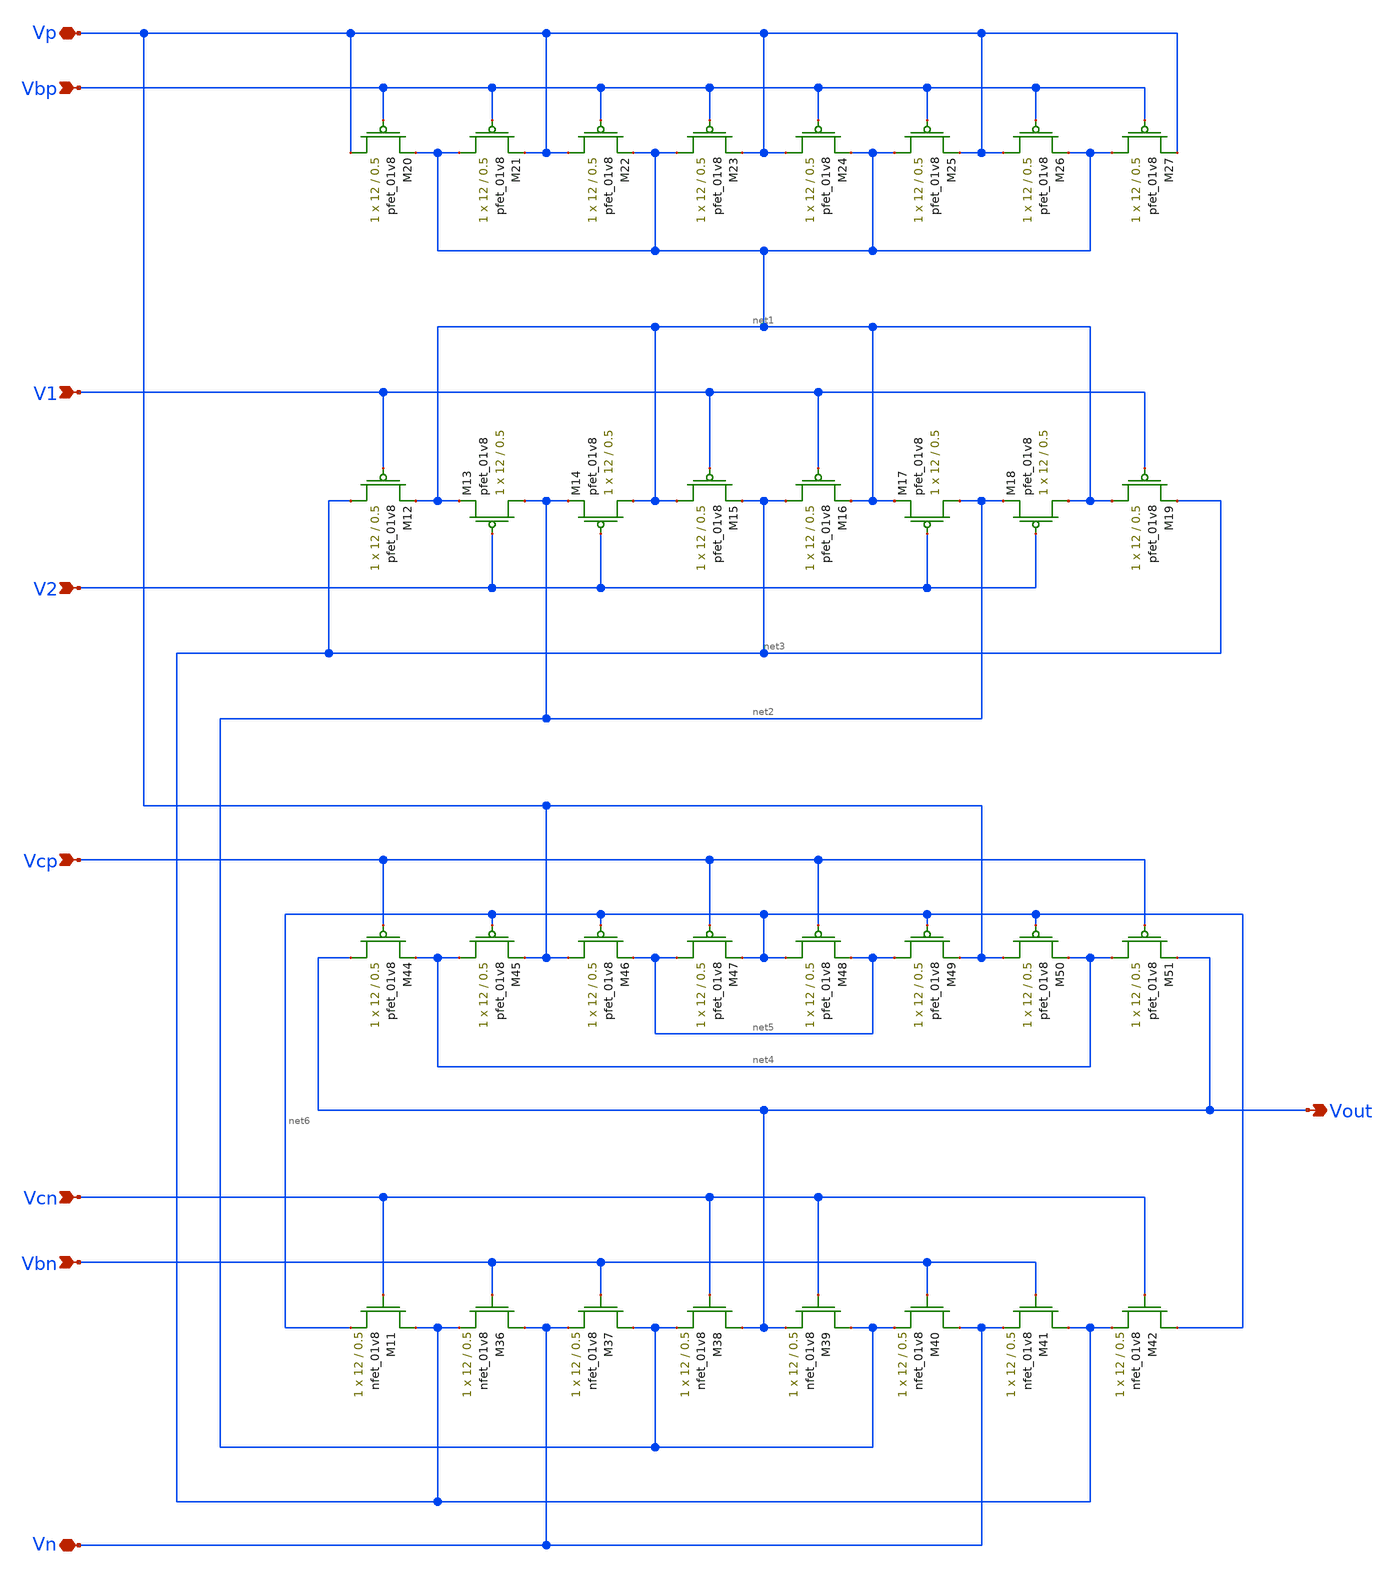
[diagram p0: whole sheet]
** sch_path: schematic/folded_cascode_differential_amplifier_LDS.sch
**.subckt folded_cascode_differential_amplifier_LDS Vbn Vcn Vcp V2 V1 Vbp Vp Vn Vout
*.ipin Vbn
*.ipin Vcn
*.ipin Vcp
*.ipin V2
*.ipin V1
*.ipin Vbp
*.iopin Vp
*.iopin Vn
*.opin Vout
XM11 net3 Vcn net6 GND sky130_fd_pr__nfet_01v8 L=0.5 W=12 nf=1 ad='int((nf+1)/2) * W/nf * 0.29' as='int((nf+2)/2) * W/nf * 0.29'
+ pd='2*int((nf+1)/2) * (W/nf + 0.29)' ps='2*int((nf+2)/2) * (W/nf + 0.29)' nrd='0.29 / W' nrs='0.29 / W'
+ sa=0 sb=0 sd=0 mult=1 m=1
XM12 net3 V1 net1 VDD sky130_fd_pr__pfet_01v8 L=0.5 W=12 nf=1 ad='int((nf+1)/2) * W/nf * 0.29' as='int((nf+2)/2) * W/nf * 0.29'
+ pd='2*int((nf+1)/2) * (W/nf + 0.29)' ps='2*int((nf+2)/2) * (W/nf + 0.29)' nrd='0.29 / W' nrs='0.29 / W'
+ sa=0 sb=0 sd=0 mult=1 m=1
XM13 net2 V2 net1 VDD sky130_fd_pr__pfet_01v8 L=0.5 W=12 nf=1 ad='int((nf+1)/2) * W/nf * 0.29' as='int((nf+2)/2) * W/nf * 0.29'
+ pd='2*int((nf+1)/2) * (W/nf + 0.29)' ps='2*int((nf+2)/2) * (W/nf + 0.29)' nrd='0.29 / W' nrs='0.29 / W'
+ sa=0 sb=0 sd=0 mult=1 m=1
XM14 net1 V2 net2 VDD sky130_fd_pr__pfet_01v8 L=0.5 W=12 nf=1 ad='int((nf+1)/2) * W/nf * 0.29' as='int((nf+2)/2) * W/nf * 0.29'
+ pd='2*int((nf+1)/2) * (W/nf + 0.29)' ps='2*int((nf+2)/2) * (W/nf + 0.29)' nrd='0.29 / W' nrs='0.29 / W'
+ sa=0 sb=0 sd=0 mult=1 m=1
XM15 net1 V1 net3 VDD sky130_fd_pr__pfet_01v8 L=0.5 W=12 nf=1 ad='int((nf+1)/2) * W/nf * 0.29' as='int((nf+2)/2) * W/nf * 0.29'
+ pd='2*int((nf+1)/2) * (W/nf + 0.29)' ps='2*int((nf+2)/2) * (W/nf + 0.29)' nrd='0.29 / W' nrs='0.29 / W'
+ sa=0 sb=0 sd=0 mult=1 m=1
XM16 net3 V1 net1 VDD sky130_fd_pr__pfet_01v8 L=0.5 W=12 nf=1 ad='int((nf+1)/2) * W/nf * 0.29' as='int((nf+2)/2) * W/nf * 0.29'
+ pd='2*int((nf+1)/2) * (W/nf + 0.29)' ps='2*int((nf+2)/2) * (W/nf + 0.29)' nrd='0.29 / W' nrs='0.29 / W'
+ sa=0 sb=0 sd=0 mult=1 m=1
XM17 net2 V2 net1 VDD sky130_fd_pr__pfet_01v8 L=0.5 W=12 nf=1 ad='int((nf+1)/2) * W/nf * 0.29' as='int((nf+2)/2) * W/nf * 0.29'
+ pd='2*int((nf+1)/2) * (W/nf + 0.29)' ps='2*int((nf+2)/2) * (W/nf + 0.29)' nrd='0.29 / W' nrs='0.29 / W'
+ sa=0 sb=0 sd=0 mult=1 m=1
XM18 net1 V2 net2 VDD sky130_fd_pr__pfet_01v8 L=0.5 W=12 nf=1 ad='int((nf+1)/2) * W/nf * 0.29' as='int((nf+2)/2) * W/nf * 0.29'
+ pd='2*int((nf+1)/2) * (W/nf + 0.29)' ps='2*int((nf+2)/2) * (W/nf + 0.29)' nrd='0.29 / W' nrs='0.29 / W'
+ sa=0 sb=0 sd=0 mult=1 m=1
XM19 net1 V1 net3 VDD sky130_fd_pr__pfet_01v8 L=0.5 W=12 nf=1 ad='int((nf+1)/2) * W/nf * 0.29' as='int((nf+2)/2) * W/nf * 0.29'
+ pd='2*int((nf+1)/2) * (W/nf + 0.29)' ps='2*int((nf+2)/2) * (W/nf + 0.29)' nrd='0.29 / W' nrs='0.29 / W'
+ sa=0 sb=0 sd=0 mult=1 m=1
XM20 Vp Vbp net1 VDD sky130_fd_pr__pfet_01v8 L=0.5 W=12 nf=1 ad='int((nf+1)/2) * W/nf * 0.29' as='int((nf+2)/2) * W/nf * 0.29'
+ pd='2*int((nf+1)/2) * (W/nf + 0.29)' ps='2*int((nf+2)/2) * (W/nf + 0.29)' nrd='0.29 / W' nrs='0.29 / W'
+ sa=0 sb=0 sd=0 mult=1 m=1
XM21 net1 Vbp Vp VDD sky130_fd_pr__pfet_01v8 L=0.5 W=12 nf=1 ad='int((nf+1)/2) * W/nf * 0.29' as='int((nf+2)/2) * W/nf * 0.29'
+ pd='2*int((nf+1)/2) * (W/nf + 0.29)' ps='2*int((nf+2)/2) * (W/nf + 0.29)' nrd='0.29 / W' nrs='0.29 / W'
+ sa=0 sb=0 sd=0 mult=1 m=1
XM22 Vp Vbp net1 VDD sky130_fd_pr__pfet_01v8 L=0.5 W=12 nf=1 ad='int((nf+1)/2) * W/nf * 0.29' as='int((nf+2)/2) * W/nf * 0.29'
+ pd='2*int((nf+1)/2) * (W/nf + 0.29)' ps='2*int((nf+2)/2) * (W/nf + 0.29)' nrd='0.29 / W' nrs='0.29 / W'
+ sa=0 sb=0 sd=0 mult=1 m=1
XM23 net1 Vbp Vp VDD sky130_fd_pr__pfet_01v8 L=0.5 W=12 nf=1 ad='int((nf+1)/2) * W/nf * 0.29' as='int((nf+2)/2) * W/nf * 0.29'
+ pd='2*int((nf+1)/2) * (W/nf + 0.29)' ps='2*int((nf+2)/2) * (W/nf + 0.29)' nrd='0.29 / W' nrs='0.29 / W'
+ sa=0 sb=0 sd=0 mult=1 m=1
XM24 Vp Vbp net1 VDD sky130_fd_pr__pfet_01v8 L=0.5 W=12 nf=1 ad='int((nf+1)/2) * W/nf * 0.29' as='int((nf+2)/2) * W/nf * 0.29'
+ pd='2*int((nf+1)/2) * (W/nf + 0.29)' ps='2*int((nf+2)/2) * (W/nf + 0.29)' nrd='0.29 / W' nrs='0.29 / W'
+ sa=0 sb=0 sd=0 mult=1 m=1
XM25 net1 Vbp Vp VDD sky130_fd_pr__pfet_01v8 L=0.5 W=12 nf=1 ad='int((nf+1)/2) * W/nf * 0.29' as='int((nf+2)/2) * W/nf * 0.29'
+ pd='2*int((nf+1)/2) * (W/nf + 0.29)' ps='2*int((nf+2)/2) * (W/nf + 0.29)' nrd='0.29 / W' nrs='0.29 / W'
+ sa=0 sb=0 sd=0 mult=1 m=1
XM26 Vp Vbp net1 VDD sky130_fd_pr__pfet_01v8 L=0.5 W=12 nf=1 ad='int((nf+1)/2) * W/nf * 0.29' as='int((nf+2)/2) * W/nf * 0.29'
+ pd='2*int((nf+1)/2) * (W/nf + 0.29)' ps='2*int((nf+2)/2) * (W/nf + 0.29)' nrd='0.29 / W' nrs='0.29 / W'
+ sa=0 sb=0 sd=0 mult=1 m=1
XM27 net1 Vbp Vp VDD sky130_fd_pr__pfet_01v8 L=0.5 W=12 nf=1 ad='int((nf+1)/2) * W/nf * 0.29' as='int((nf+2)/2) * W/nf * 0.29'
+ pd='2*int((nf+1)/2) * (W/nf + 0.29)' ps='2*int((nf+2)/2) * (W/nf + 0.29)' nrd='0.29 / W' nrs='0.29 / W'
+ sa=0 sb=0 sd=0 mult=1 m=1
XM36 Vn Vbn net3 GND sky130_fd_pr__nfet_01v8 L=0.5 W=12 nf=1 ad='int((nf+1)/2) * W/nf * 0.29' as='int((nf+2)/2) * W/nf * 0.29'
+ pd='2*int((nf+1)/2) * (W/nf + 0.29)' ps='2*int((nf+2)/2) * (W/nf + 0.29)' nrd='0.29 / W' nrs='0.29 / W'
+ sa=0 sb=0 sd=0 mult=1 m=1
XM37 net2 Vbn Vn GND sky130_fd_pr__nfet_01v8 L=0.5 W=12 nf=1 ad='int((nf+1)/2) * W/nf * 0.29' as='int((nf+2)/2) * W/nf * 0.29'
+ pd='2*int((nf+1)/2) * (W/nf + 0.29)' ps='2*int((nf+2)/2) * (W/nf + 0.29)' nrd='0.29 / W' nrs='0.29 / W'
+ sa=0 sb=0 sd=0 mult=1 m=1
XM38 Vout Vcn net2 GND sky130_fd_pr__nfet_01v8 L=0.5 W=12 nf=1 ad='int((nf+1)/2) * W/nf * 0.29' as='int((nf+2)/2) * W/nf * 0.29'
+ pd='2*int((nf+1)/2) * (W/nf + 0.29)' ps='2*int((nf+2)/2) * (W/nf + 0.29)' nrd='0.29 / W' nrs='0.29 / W'
+ sa=0 sb=0 sd=0 mult=1 m=1
XM39 net2 Vcn Vout GND sky130_fd_pr__nfet_01v8 L=0.5 W=12 nf=1 ad='int((nf+1)/2) * W/nf * 0.29' as='int((nf+2)/2) * W/nf * 0.29'
+ pd='2*int((nf+1)/2) * (W/nf + 0.29)' ps='2*int((nf+2)/2) * (W/nf + 0.29)' nrd='0.29 / W' nrs='0.29 / W'
+ sa=0 sb=0 sd=0 mult=1 m=1
XM40 Vn Vbn net2 GND sky130_fd_pr__nfet_01v8 L=0.5 W=12 nf=1 ad='int((nf+1)/2) * W/nf * 0.29' as='int((nf+2)/2) * W/nf * 0.29'
+ pd='2*int((nf+1)/2) * (W/nf + 0.29)' ps='2*int((nf+2)/2) * (W/nf + 0.29)' nrd='0.29 / W' nrs='0.29 / W'
+ sa=0 sb=0 sd=0 mult=1 m=1
XM41 net3 Vbn Vn GND sky130_fd_pr__nfet_01v8 L=0.5 W=12 nf=1 ad='int((nf+1)/2) * W/nf * 0.29' as='int((nf+2)/2) * W/nf * 0.29'
+ pd='2*int((nf+1)/2) * (W/nf + 0.29)' ps='2*int((nf+2)/2) * (W/nf + 0.29)' nrd='0.29 / W' nrs='0.29 / W'
+ sa=0 sb=0 sd=0 mult=1 m=1
XM42 net6 Vcn net3 GND sky130_fd_pr__nfet_01v8 L=0.5 W=12 nf=1 ad='int((nf+1)/2) * W/nf * 0.29' as='int((nf+2)/2) * W/nf * 0.29'
+ pd='2*int((nf+1)/2) * (W/nf + 0.29)' ps='2*int((nf+2)/2) * (W/nf + 0.29)' nrd='0.29 / W' nrs='0.29 / W'
+ sa=0 sb=0 sd=0 mult=1 m=1
XM44 Vout Vcp net4 VDD sky130_fd_pr__pfet_01v8 L=0.5 W=12 nf=1 ad='int((nf+1)/2) * W/nf * 0.29' as='int((nf+2)/2) * W/nf * 0.29'
+ pd='2*int((nf+1)/2) * (W/nf + 0.29)' ps='2*int((nf+2)/2) * (W/nf + 0.29)' nrd='0.29 / W' nrs='0.29 / W'
+ sa=0 sb=0 sd=0 mult=1 m=1
XM45 net4 net6 Vp VDD sky130_fd_pr__pfet_01v8 L=0.5 W=12 nf=1 ad='int((nf+1)/2) * W/nf * 0.29' as='int((nf+2)/2) * W/nf * 0.29'
+ pd='2*int((nf+1)/2) * (W/nf + 0.29)' ps='2*int((nf+2)/2) * (W/nf + 0.29)' nrd='0.29 / W' nrs='0.29 / W'
+ sa=0 sb=0 sd=0 mult=1 m=1
XM46 Vp net6 net5 VDD sky130_fd_pr__pfet_01v8 L=0.5 W=12 nf=1 ad='int((nf+1)/2) * W/nf * 0.29' as='int((nf+2)/2) * W/nf * 0.29'
+ pd='2*int((nf+1)/2) * (W/nf + 0.29)' ps='2*int((nf+2)/2) * (W/nf + 0.29)' nrd='0.29 / W' nrs='0.29 / W'
+ sa=0 sb=0 sd=0 mult=1 m=1
XM47 net5 Vcp net6 VDD sky130_fd_pr__pfet_01v8 L=0.5 W=12 nf=1 ad='int((nf+1)/2) * W/nf * 0.29' as='int((nf+2)/2) * W/nf * 0.29'
+ pd='2*int((nf+1)/2) * (W/nf + 0.29)' ps='2*int((nf+2)/2) * (W/nf + 0.29)' nrd='0.29 / W' nrs='0.29 / W'
+ sa=0 sb=0 sd=0 mult=1 m=1
XM48 net6 Vcp net5 VDD sky130_fd_pr__pfet_01v8 L=0.5 W=12 nf=1 ad='int((nf+1)/2) * W/nf * 0.29' as='int((nf+2)/2) * W/nf * 0.29'
+ pd='2*int((nf+1)/2) * (W/nf + 0.29)' ps='2*int((nf+2)/2) * (W/nf + 0.29)' nrd='0.29 / W' nrs='0.29 / W'
+ sa=0 sb=0 sd=0 mult=1 m=1
XM49 net5 net6 Vp VDD sky130_fd_pr__pfet_01v8 L=0.5 W=12 nf=1 ad='int((nf+1)/2) * W/nf * 0.29' as='int((nf+2)/2) * W/nf * 0.29'
+ pd='2*int((nf+1)/2) * (W/nf + 0.29)' ps='2*int((nf+2)/2) * (W/nf + 0.29)' nrd='0.29 / W' nrs='0.29 / W'
+ sa=0 sb=0 sd=0 mult=1 m=1
XM50 Vp net6 net4 VDD sky130_fd_pr__pfet_01v8 L=0.5 W=12 nf=1 ad='int((nf+1)/2) * W/nf * 0.29' as='int((nf+2)/2) * W/nf * 0.29'
+ pd='2*int((nf+1)/2) * (W/nf + 0.29)' ps='2*int((nf+2)/2) * (W/nf + 0.29)' nrd='0.29 / W' nrs='0.29 / W'
+ sa=0 sb=0 sd=0 mult=1 m=1
XM51 net4 Vcp Vout VDD sky130_fd_pr__pfet_01v8 L=0.5 W=12 nf=1 ad='int((nf+1)/2) * W/nf * 0.29' as='int((nf+2)/2) * W/nf * 0.29'
+ pd='2*int((nf+1)/2) * (W/nf + 0.29)' ps='2*int((nf+2)/2) * (W/nf + 0.29)' nrd='0.29 / W' nrs='0.29 / W'
+ sa=0 sb=0 sd=0 mult=1 m=1
**.ends
.end
